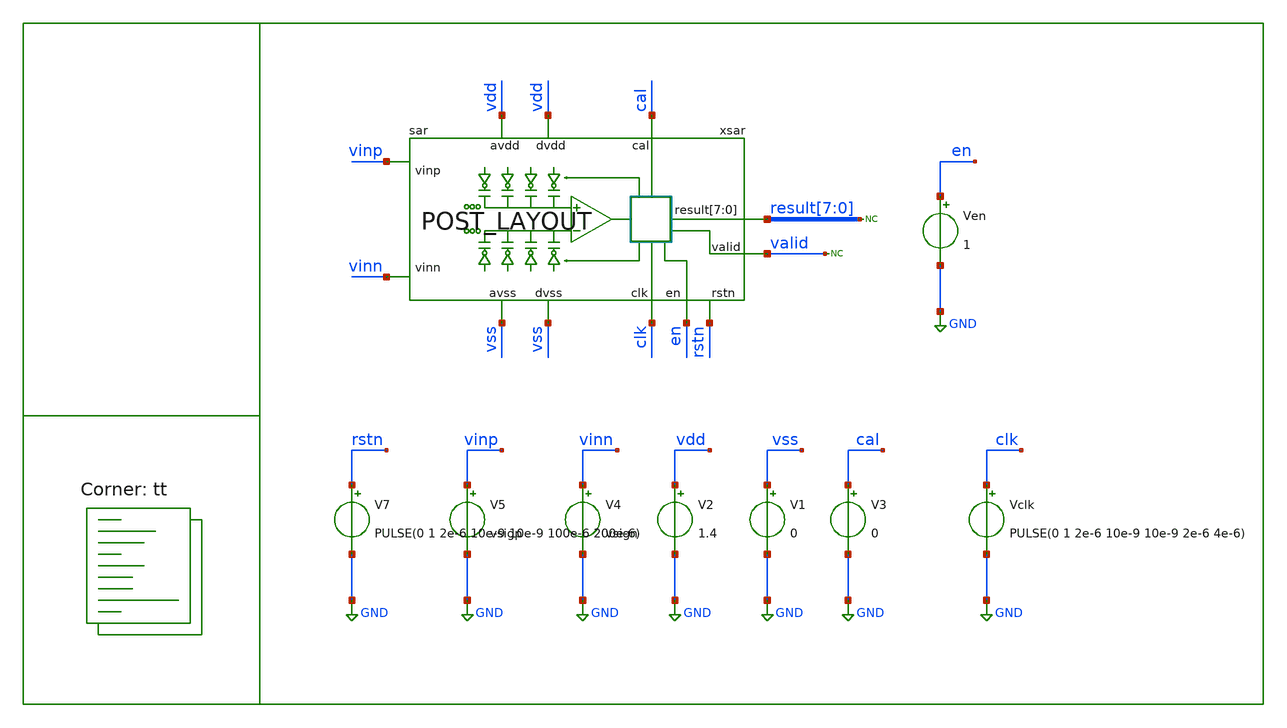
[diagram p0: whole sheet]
** sch_path: xschem/tb/sar/tr_sar.sch

.include $::SKYWATER_STDCELLS/sky130_fd_sc_hd.spice
*.include $::SKYWATER_STDCELLS/cells/inv/sky130_fd_sc_hd__inv_4.spice
*.include $::SKYWATER_STDCELLS/cells/decap/sky130_fd_sc_hd__decap_8.spice
*.include $::SKYWATER_STDCELLS/cells/decap/sky130_fd_sc_hd__decap_3.spice
*.include $::SKYWATER_STDCELLS/cells/buf/sky130_fd_sc_hd__buf_1.spice
*.include $::SKYWATER_STDCELLS/cells/inv/sky130_fd_sc_hd__inv_1.spice
*.include $::SKYWATER_STDCELLS/cells/inv/sky130_fd_sc_hd__inv_2.spice
*.include $::SKYWATER_STDCELLS/cells/tap/sky130_fd_sc_hd__tap_2.spice

.lib $::SKYWATER_MODELS/sky130.lib.spice tt
**.subckt tr_sar
V1 vss GND 0
V2 vdd GND 1.4
V4 vinn GND vsign
V5 vinp GND vsigp
Vclk clk GND PULSE(0 1 2e-6 10e-9 10e-9 2e-6 4e-6)
Ven en GND 1
* noconn valid
V3 cal GND 0
* noconn result[7:0]
xsar vdd vdd vss result[7] result[6] result[5] result[4] result[3] result[2] result[1] result[0]
+ vinn vss clk vinp en valid cal rstn sar
V7 rstn GND PULSE(0 1 2e-6 10e-9 10e-9 100e-6 200e-6)
**.ends

* expanding   symbol:  sar/sar/sar.sym # of pins=12
** sym_path: xschem/sar/SAR_POSTLAYOUT/sar.sym
** sch_path: xschem/sar/SAR_POSTLAYOUT/sar.sch
.subckt sar avdd dvdd dvss result[7] result[6] result[5] result[4] result[3] result[2] result[1]
+ result[0] vinn avss clk vinp en valid cal rstn
*.iopin avss
*.iopin avdd
*.iopin dvss
*.iopin dvdd
*.ipin vinp
*.ipin vinn
*.opin result[7],result[6],result[5],result[4],result[3],result[2],result[1],result[0]
*.ipin clk
*.ipin en
*.opin valid
*.ipin cal
*.ipin rstn
* noconn comp
**** begin user architecture code

*.include $::DESIGN_PATH/sar/control/cmos_cells_digital.sp
*.include $::DESIGN_PATH/sar/control/sar_logic.sp
*.include $::DESIGN_PATH/sar/control/sar_logic_sky.sp
.include $::DESIGN_PATH/sar/SAR_POSTLAYOUT/user_analog_project_wrapper.spice

**** end user architecture code
* noconn sample
* noconn ctln[7:0]
* noconn ctlp[7:0]
* noconn trim[4:0]
* noconn trimb[4:0]
* noconn result[7:0]
* noconn valid
* noconn clkc
* noconn clk
* noconn en
* noconn cal
* noconn rstn
**** begin user architecture code


**Xuut dclk drstn den dcomp dcal dvalid dres0 dres1 dres2 dres3 dres4 dres5 dres6 dres7 dsamp dctlp0
*+ dctlp1 dctlp2 dctlp3 dctlp4 dctlp5 dctlp6 dctlp7 dctln0 dctln1 dctln2 dctln3 dctln4 dctln5 dctln6 dctln7
*+ dtrim0 dtrim1 dtrim2 dtrim3 dtrim4 dtrimb0 dtrimb1 dtrimb2 dtrimb3 dtrimb4 dclkc sar_logic

.model adc_buff adc_bridge(in_low = 0.2 in_high=0.8)
.model dac_buff dac_bridge(out_high = 1.2)

Aad [clk rstn en comp cal] [dclk drstn den dcomp dcal] adc_buff
Ada [dctlp0 dctlp1 dctlp2 dctlp3 dctlp4 dctlp5 dctlp6 dctlp7 dctln0 dctln1 dctln2 dctln3 dctln4
+ dctln5 dctln6 dctln7 dres0 dres1 dres2 dres3 dres4 dres5 dres6 dres7 dsamp dclkc] [ctlp_0_ ctlp_1_ ctlp_2_
+ ctlp_3_ ctlp_4_ ctlp_5_ ctlp_6_ ctlp_7_ ctln_0_ ctln_1_ ctln_2_ ctln_3_ ctln_4_ ctln_5_ ctln_6_ ctln_7_
+ res0 res1 res2 res3 res4 res5 res6 res7 sample clkc] dac_buff
Ada2 [dtrim4 dtrim3 dtrim2 dtrim1 dtrim0 dtrimb4 dtrimb3 dtrimb2 dtrimb1 dtrimb0] [trim_4_ trim_3_
+ trim_2_ trim_1_ trim_0_ trimb_4_ trimb_3_ trimb_2_ trimb_1_ trimb_0_ ] dac_buff


xsar dcomp dctln1 dctln0 dctlp1 dctlp0 dctln7 dctln6 dctln5 dctln4 dctln3 dctln2 dtrim4  dtrim1
+ dtrim0 dtrim2 dtrim3 dtrimb3 dtrimb2 dtrimb0 dtrimb1 dtrimb4 dctlp2 dctlp3 dctlp4 dctlp5  dctlp6 dctlp7
+ dclkc dres7 dres6 dres5 dres4 drstn dres3 dres2 dres1 dres0  dvalid dcal den dclk vinp vinn dvdd avdd
+ dvss SAR


**** end user architecture code
.ends

.GLOBAL GND
**** begin user architecture code
 *.options method trap
.options method=gear
.options gmin=1e-6
.options abstol=1e-8
.options reltol=0.01
.options vntol=1e-6
.options warn=1

.param MC_SWITCH=0
.param vin=1
.param vcm=0.7
.param vsigp=1.2
.param vsign=0.2
.param VPWR=1.8
.param VGND=0
.param VPB=1.8
.param VNB=0
.tran 100e-9 48e-6

.control

save all
run
write tr_sar.raw

.endc
**** end user architecture code
.end
